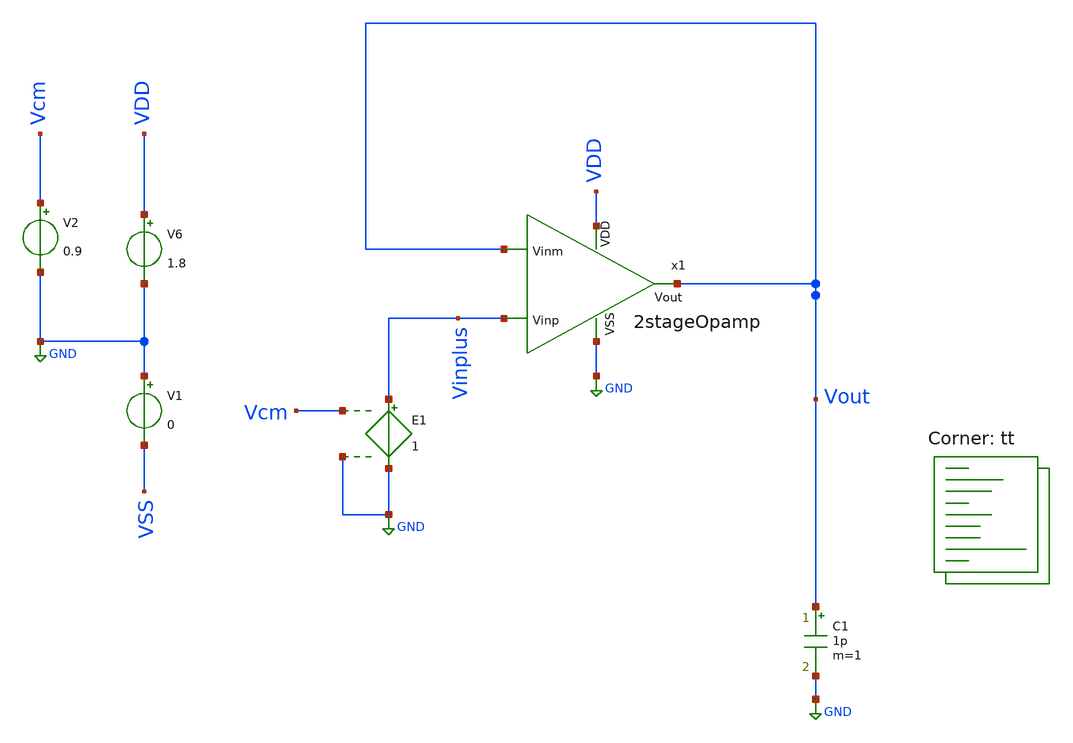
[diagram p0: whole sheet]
** sch_path: xschem/TestBenches/ICMRtb.sch
**.subckt ICMRtb
V2 Vcm GND 0.9
C1 Vout GND 1p m=1
V6 VDD GND 1.8
E1 Vinplus GND Vcm GND 1
V1 GND VSS 0
x1 VDD Vout Vinplus Vout GND 2stageOpamp
**** begin user architecture code
.lib $::SKYWATER_MODELS/sky130.lib.spice tt

* this option enables mos model bin
* selection based on W/NF instead of W
.option wnflag=1
.option savecurrents

.control
save all
save @x1.m.xm5.msky130_fd_pr__nfet_01v8[gm]
save @x1.m.xm5.msky130_fd_pr__nfet_01v8[gds]
save @x1.m.xm5.msky130_fd_pr__nfet_01v8[id]
save @x1.m.xm5.msky130_fd_pr__nfet_01v8[vth]
save @x1.m.xm5.msky130_fd_pr__nfet_01v8[vgs]
save @x1.m.xm5.msky130_fd_pr__nfet_01v8[vds]

save @x1.m.xm4.msky130_fd_pr__pfet_01v8_lvt[gds]
save @x1.m.xm4.msky130_fd_pr__pfet_01v8_lvt[gm]
save @x1.m.xm4.msky130_fd_pr__pfet_01v8_lvt[id]
save @x1.m.xm4.msky130_fd_pr__pfet_01v8_lvt[vth]
save @x1.m.xm4.msky130_fd_pr__pfet_01v8_lvt[vds]
save @x1.m.xm4.msky130_fd_pr__pfet_01v8_lvt[vgs]

save @x1.m.xm3.msky130_fd_pr__pfet_01v8_lvt[gm]
save @x1.m.xm3.msky130_fd_pr__pfet_01v8_lvt[gds]
save @x1.m.xm3.msky130_fd_pr__pfet_01v8_lvt[id]
save @x1.m.xm4.msky130_fd_pr__pfet_01v8_lvt[vth]
save @x1.m.xm4.msky130_fd_pr__pfet_01v8_lvt[vds]
save @x1.m.xm4.msky130_fd_pr__pfet_01v8_lvt[vgs]


dc V2 0 1.8 0.01
let dVout = deriv(Vout)
let dVcm = deriv(Vinplus)

plot Vout
plot Vinplus
plot Vinminus
plot dVcm/dVout
plot dVout
plot @x1.m.xm5.msky130_fd_pr__nfet_01v8[gm]
plot @x1.m.xm5.msky130_fd_pr__nfet_01v8[gds]
plot @x1.m.xm5.msky130_fd_pr__nfet_01v8[id]

plot @x1.m.xm4.msky130_fd_pr__pfet_01v8_lvt[gds]
plot @x1.m.xm4.msky130_fd_pr__pfet_01v8_lvt[gm]
plot @x1.m.xm4.msky130_fd_pr__pfet_01v8_lvt[id]

plot @x1.m.xm3.msky130_fd_pr__pfet_01v8_lvt[gm]
plot @x1.m.xm3.msky130_fd_pr__pfet_01v8_lvt[gds]
plot @x1.m.xm3.msky130_fd_pr__pfet_01v8_lvt[id]



 set appendwrite
 set filetype=binary
 write ICMRtb.raw

.endc


**** end user architecture code
**.ends
.GLOBAL GND
.end
